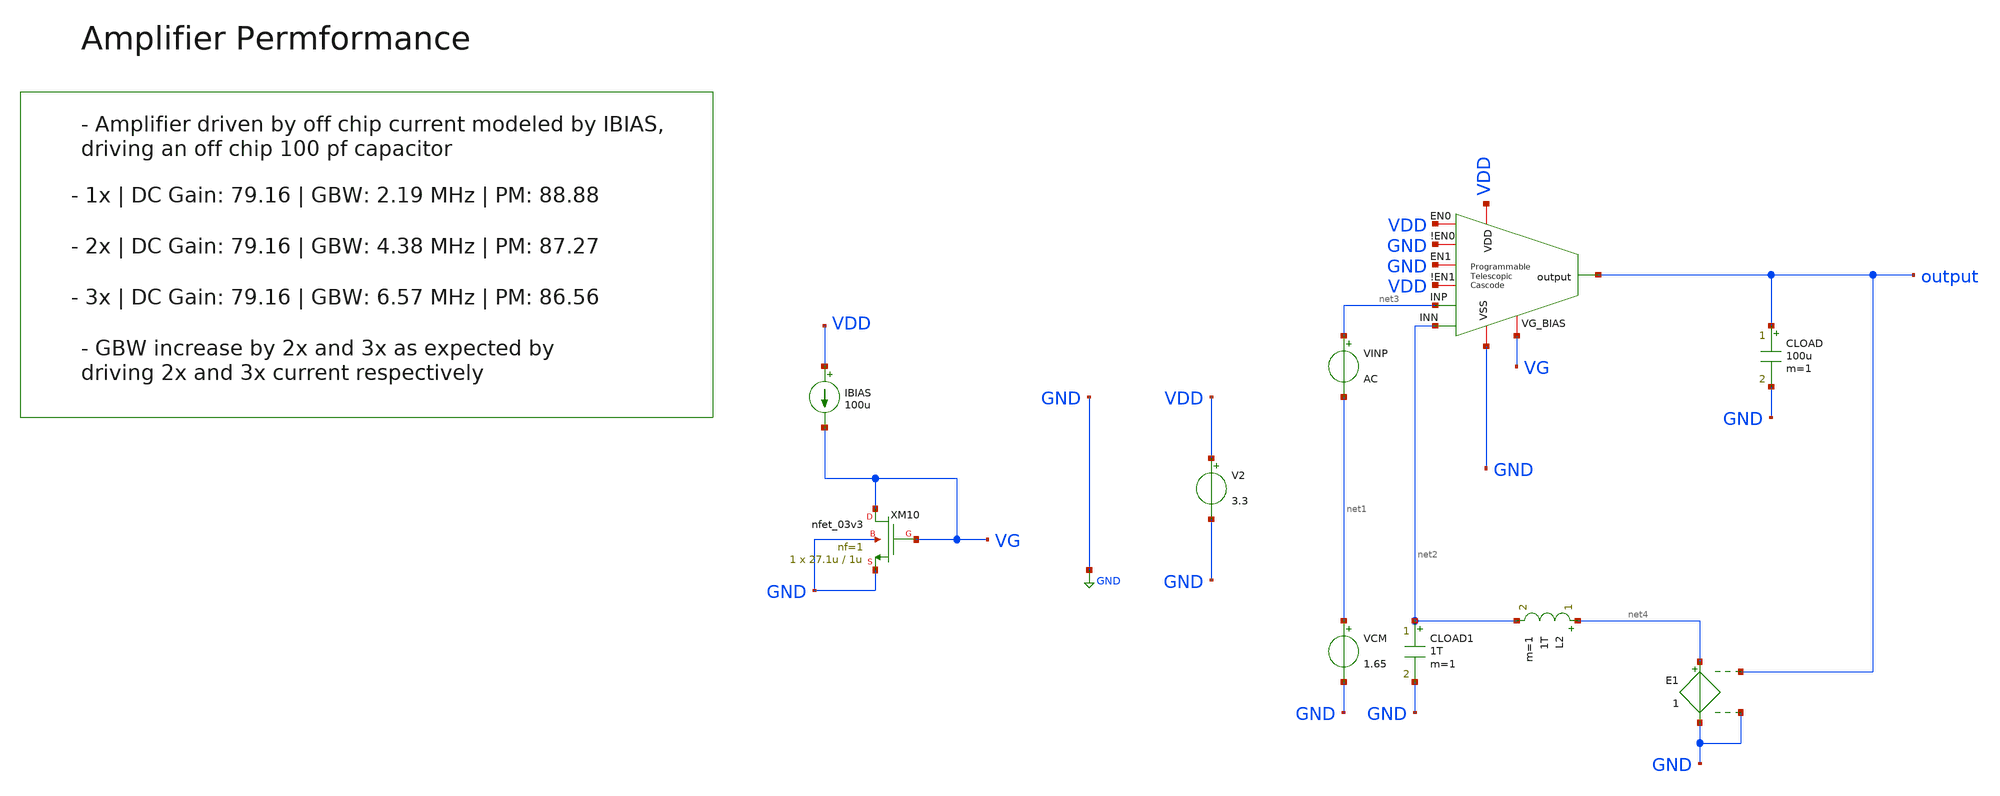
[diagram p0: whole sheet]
** sch_path: designs/libs/core_amps/ota_telescopic/programmable_tb/programmable_telescopic_cascode_ac_open_tb.sch
**.subckt programmable_telescopic_cascode_ac_open_tb
IBIAS VDD VG 100u
V2 VDD GND 3.3
CLOAD output GND 100u m=1
VINP net3 net1 AC
VCM net1 GND 1.65
L2 net4 net2 1T m=1
CLOAD1 net2 GND 1T m=1
E1 net4 GND output GND 1
XM10 VG VG GND GND nfet_03v3 L=1u W=27.1u nf=1 ad='int((nf+1)/2) * W/nf * 0.18u' as='int((nf+2)/2) * W/nf * 0.18u'
+ pd='2*int((nf+1)/2) * (W/nf + 0.18u)' ps='2*int((nf+2)/2) * (W/nf + 0.18u)' nrd='0.18u / W' nrs='0.18u / W'
+ sa=0 sb=0 sd=0 m=1
x1 VDD output VDD GND GND VDD net2 net3 GND VG programmable_telescopic_cascode
**** begin user architecture code

.include $::180MCU_MODELS/design.ngspice
.lib $::180MCU_MODELS/sm141064.ngspice typical



.control
ac dec 100 1 1G

plot vdb(output) ph(v(output))*180/3.14159

meas ac dc_gain find vdb(output) at=1
meas ac gbw when vdb(output)=0
let gain_db = vdb(output)
let phase = 180/3.14159*ph(v(output))
meas ac phase_at_gbw find phase when vdb(output)=0
let pm = 180 + phase_at_gbw
print pm

.endc



**** end user architecture code
**.ends
.GLOBAL GND
.end
